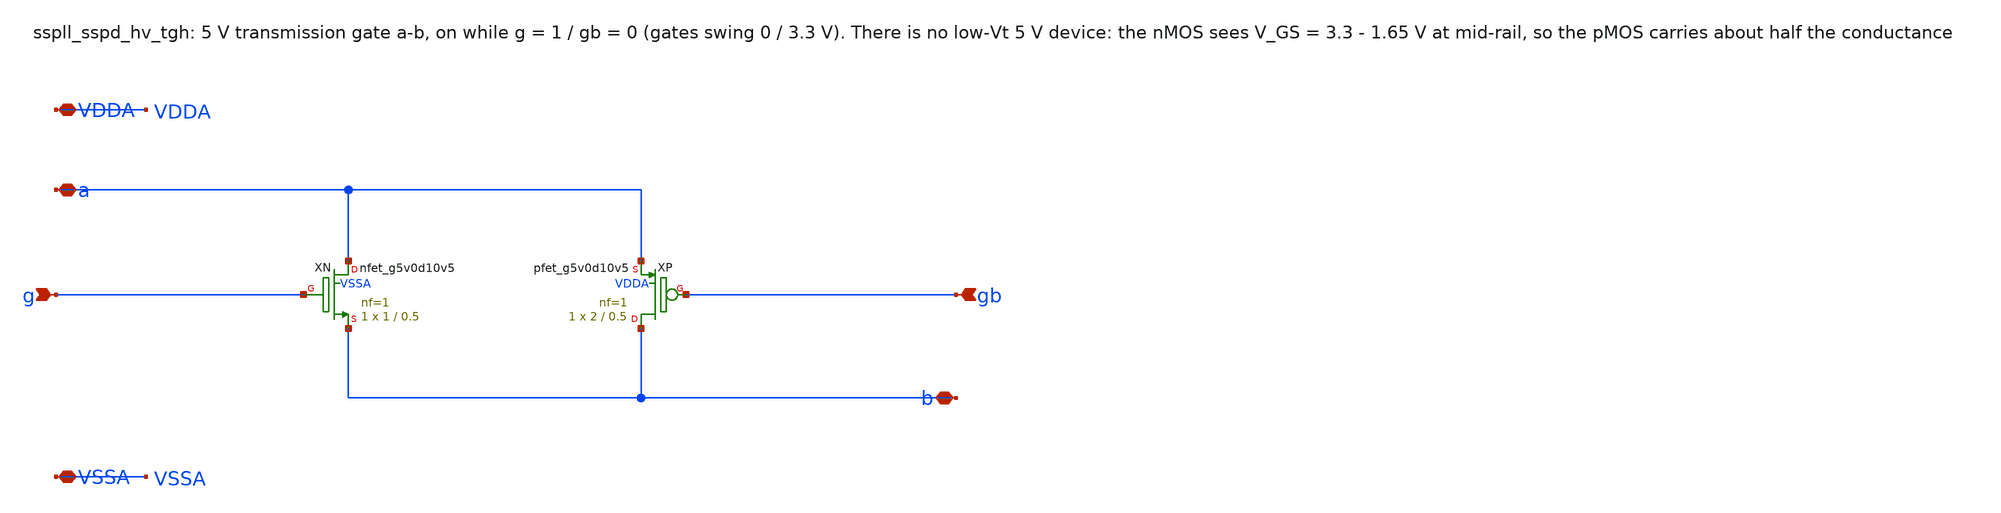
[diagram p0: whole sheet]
** sch_path: xschem/sspd_hv/sspll_sspd_hv_tgh.sch
**.subckt sspll_sspd_hv_tgh a b g gb VDDA VSSA
*.iopin a
*.iopin b
*.ipin g
*.ipin gb
*.iopin VDDA
*.iopin VSSA
XXN a g b VSSA sky130_fd_pr__nfet_g5v0d10v5 L=0.5 W=1 nf=1 ad='int((nf+1)/2) * W/nf * 0.29' as='int((nf+2)/2) * W/nf * 0.29'
+ pd='2*int((nf+1)/2) * (W/nf + 0.29)' ps='2*int((nf+2)/2) * (W/nf + 0.29)' nrd='0.29 / W' nrs='0.29 / W'
+ sa=0 sb=0 sd=0 mult=1 m=1
XXP b gb a VDDA sky130_fd_pr__pfet_g5v0d10v5 L=0.5 W=2 nf=1 ad='int((nf+1)/2) * W/nf * 0.29' as='int((nf+2)/2) * W/nf * 0.29'
+ pd='2*int((nf+1)/2) * (W/nf + 0.29)' ps='2*int((nf+2)/2) * (W/nf + 0.29)' nrd='0.29 / W' nrs='0.29 / W'
+ sa=0 sb=0 sd=0 mult=1 m=1
**.ends
.end
